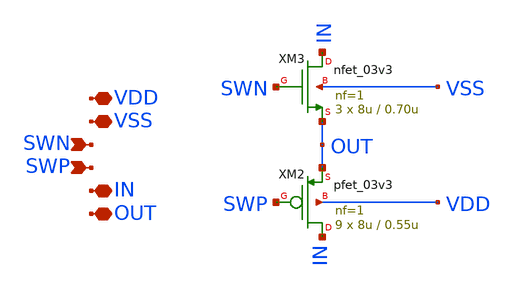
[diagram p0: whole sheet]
** sch_path: designs/libs/core_switch-matrix/trans-gate/trans-gate.sch
**.subckt trans-gate VDD VSS IN OUT SWN SWP
*.iopin VDD
*.iopin VSS
*.iopin IN
*.iopin OUT
*.ipin SWN
*.ipin SWP
XM3 IN SWN OUT VSS nfet_03v3 L=0.70u W=8u nf=1 ad='int((nf+1)/2) * W/nf * 0.18u' as='int((nf+2)/2) * W/nf * 0.18u'
+ pd='2*int((nf+1)/2) * (W/nf + 0.18u)' ps='2*int((nf+2)/2) * (W/nf + 0.18u)' nrd='0.18u / W' nrs='0.18u / W'
+ sa=0 sb=0 sd=0 m=3
XM2 IN SWP OUT VDD pfet_03v3 L=0.55u W=8u nf=1 ad='int((nf+1)/2) * W/nf * 0.18u' as='int((nf+2)/2) * W/nf * 0.18u'
+ pd='2*int((nf+1)/2) * (W/nf + 0.18u)' ps='2*int((nf+2)/2) * (W/nf + 0.18u)' nrd='0.18u / W' nrs='0.18u / W'
+ sa=0 sb=0 sd=0 m=9
**.ends
.end
